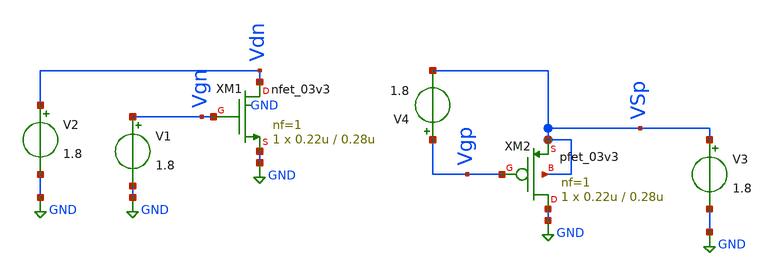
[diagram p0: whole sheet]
** sch_path: xschem/caracterizador/charac.sch
* Copyright 2022 GlobalFoundries PDK Authors
* Licensed under the Apache License, Version 2.0 (the "License");
* you may not use this file except in compliance with the License.
* You may obtain a copy of the License at
* https://www.apache.org/licenses/LICENSE-2.0
* Unless required by applicable law or agreed to in writing, software
* distributed under the License is distributed on an "AS IS" BASIS,
* WITHOUT WARRANTIES OR CONDITIONS OF ANY KIND, either express or implied.
* See the License for the specific language governing permissions and
* limitations under the License.
**.subckt charac
XM1 Vdn Vgn GND GND nfet_03v3 L=0.28u W=0.22u nf=1 ad='int((nf+1)/2) * W/nf * 0.18u' as='int((nf+2)/2) * W/nf * 0.18u'
+ pd='2*int((nf+1)/2) * (W/nf + 0.18u)' ps='2*int((nf+2)/2) * (W/nf + 0.18u)' nrd='0.18u / W' nrs='0.18u / W'
+ sa=0 sb=0 sd=0 m=1 par=1
XM2 GND Vgp VSp VSp pfet_03v3 L=0.28u W=0.22u nf=1 ad='int((nf+1)/2) * W/nf * 0.18u' as='int((nf+2)/2) * W/nf * 0.18u'
+ pd='2*int((nf+1)/2) * (W/nf + 0.18u)' ps='2*int((nf+2)/2) * (W/nf + 0.18u)' nrd='0.18u / W' nrs='0.18u / W'
+ sa=0 sb=0 sd=0 m=1 par=1
V1 Vgn GND 1.8
V2 Vdn GND 1.8
V3 VSp GND 1.8
V4 Vgp VSp 1.8
**** begin user architecture code


.include /home/ringosinye/eda/pdks/gf180mcuD/libs.tech/ngspice/design.ngspice
.lib /home/ringosinye/eda/pdks/gf180mcuD/libs.tech/ngspice/sm141064.ngspice typical
.param sw_stat_mismatch = 0


**** end user architecture code
**.ends
.GLOBAL GND
.end
